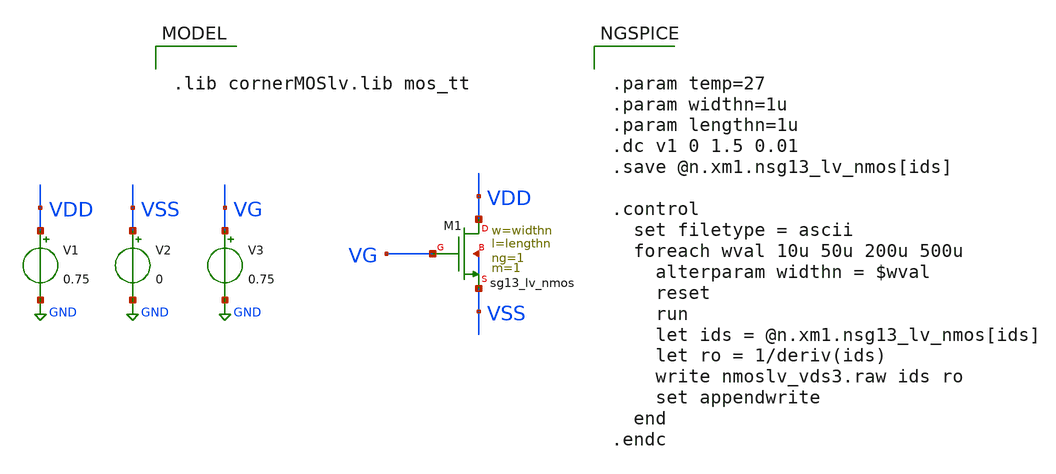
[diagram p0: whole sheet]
** sch_path: analog/tb/tb_nmos_lv_vds.sch
**.subckt tb_nmos_lv_vds
V1 VDD GND 0.75
V2 VSS GND 0
V3 VG GND 0.75
XM1 VDD VG VSS VSS sg13_lv_nmos w=widthn l=lengthn ng=1 m=1 mm_ok=1
**** begin user architecture code


.param temp=27
.param widthn=1u
.param lengthn=1u
.dc v1 0 1.5 0.01
.save @n.xm1.nsg13_lv_nmos[ids]

.control
  set filetype = ascii
  foreach wval 10u 50u 200u 500u
    alterparam widthn = $wval
    reset
    run
    let ids = @n.xm1.nsg13_lv_nmos[ids]
    let ro = 1/deriv(ids)
    write nmoslv_vds3.raw ids ro
    set appendwrite
  end
.endc





.lib cornerMOSlv.lib mos_tt


**** end user architecture code
**.ends
.GLOBAL GND
.end
